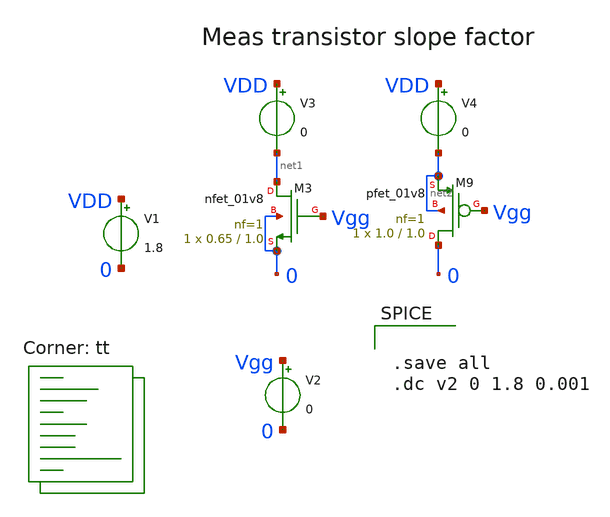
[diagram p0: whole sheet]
** sch_path: design/xschem/slopefactor.sch
**.subckt slopefactor
XM3 net1 Vgg 0 0 sky130_fd_pr__nfet_01v8 L=1.0 W=0.65 nf=1 ad='int((nf+1)/2) * W/nf * 0.29' as='int((nf+2)/2) * W/nf * 0.29'
+ pd='2*int((nf+1)/2) * (W/nf + 0.29)' ps='2*int((nf+2)/2) * (W/nf + 0.29)' nrd='0.29 / W' nrs='0.29 / W'
+ sa=0 sb=0 sd=0 mult=1 m=1
XM9 0 Vgg net2 net2 sky130_fd_pr__pfet_01v8 L=1.0 W=1.0 nf=1 ad='int((nf+1)/2) * W/nf * 0.29' as='int((nf+2)/2) * W/nf * 0.29'
+ pd='2*int((nf+1)/2) * (W/nf + 0.29)' ps='2*int((nf+2)/2) * (W/nf + 0.29)' nrd='0.29 / W' nrs='0.29 / W'
+ sa=0 sb=0 sd=0 mult=1 m=1
V1 VDD 0 1.8
V2 Vgg 0 0
V3 VDD net1 0
V4 VDD net2 0
**** begin user architecture code
.lib $::SKYWATER_MODELS/sky130.lib.spice tt


.save all
.dc v2 0 1.8 0.001


**** end user architecture code
**.ends
.end
